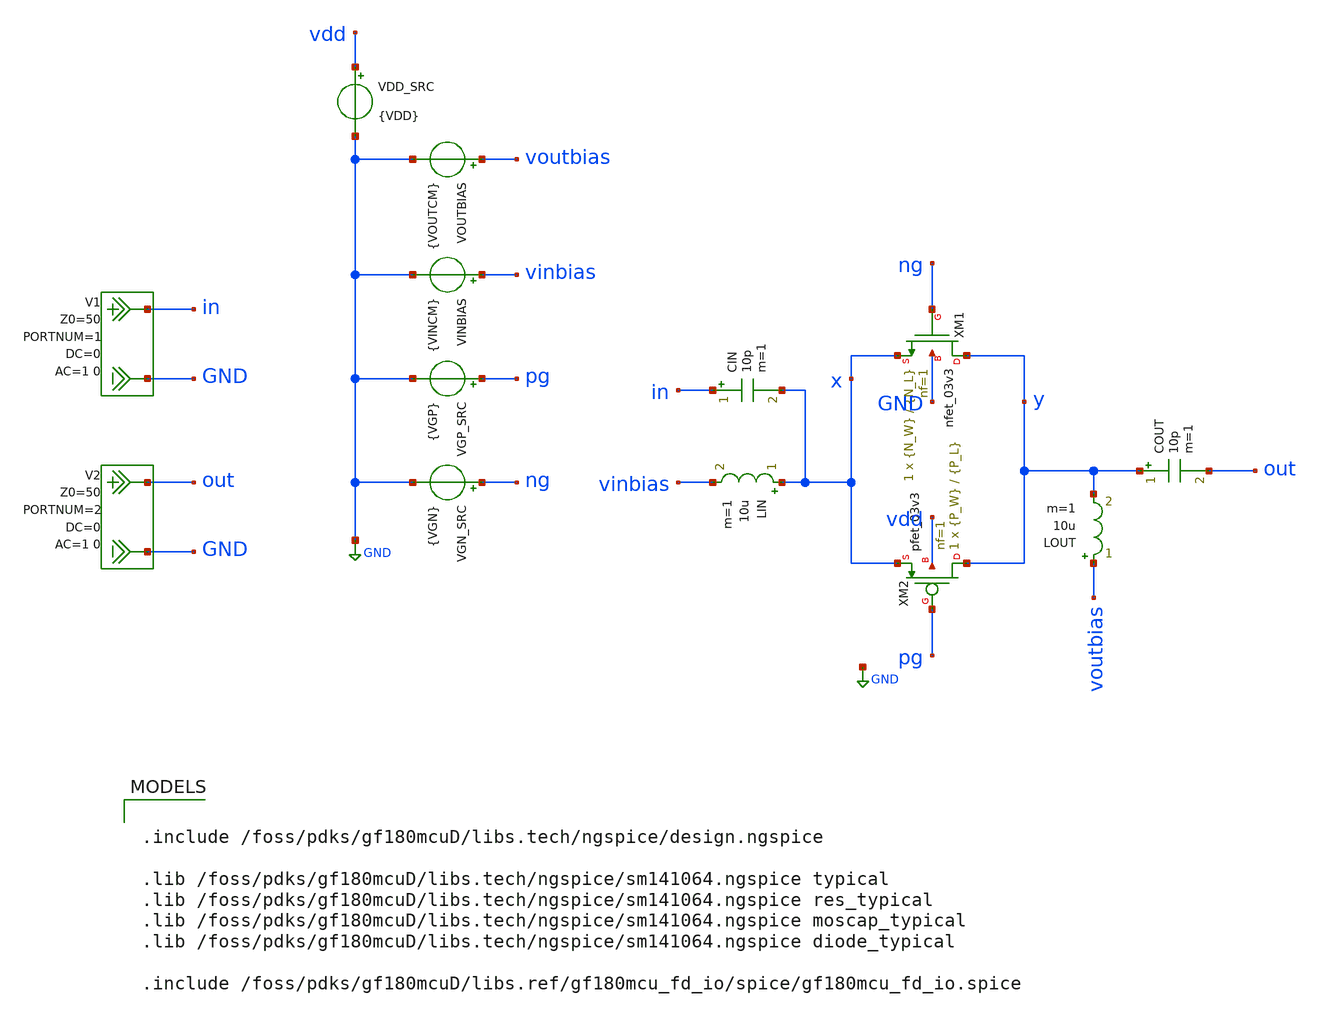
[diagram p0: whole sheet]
** sch_path: NFmin_Simulation/simulations/03_cmos/nfmin_jd_cmos_tg_cg.sch
**.subckt nfmin_jd_cmos_tg_cg
VGN_SRC ng GND {VGN}
VDD_SRC vdd GND {VDD}
COUT y out 10p m=1
CIN in x 10p m=1
XM2 y pg x vdd pfet_03v3 L={P_L} W={P_W} nf=1 ad='int((nf+1)/2) * W/nf * 0.18u' as='int((nf+2)/2) * W/nf * 0.18u'
+ pd='2*int((nf+1)/2) * (W/nf + 0.18u)' ps='2*int((nf+2)/2) * (W/nf + 0.18u)' nrd='0.18u / W' nrs='0.18u / W'
+ sa=0 sb=0 sd=0 m=1
XM1 y ng x GND nfet_03v3 L={N_L} W={N_W} nf=1 ad='int((nf+1)/2) * W/nf * 0.18u' as='int((nf+2)/2) * W/nf * 0.18u'
+ pd='2*int((nf+1)/2) * (W/nf + 0.18u)' ps='2*int((nf+2)/2) * (W/nf + 0.18u)' nrd='0.18u / W' nrs='0.18u / W'
+ sa=0 sb=0 sd=0 m=1
V1 in GND DC 0 AC 1 0 portnum 1 z0 50
V2 out GND DC 0 AC 1 0 portnum 2 z0 50
LIN x vinbias 10u m=1
VGP_SRC pg GND {VGP}
VINBIAS vinbias GND {VINCM}
VOUTBIAS voutbias GND {VOUTCM}
LOUT voutbias y 10u m=1
**** begin user architecture code

.include /foss/pdks/gf180mcuD/libs.tech/ngspice/design.ngspice

.lib /foss/pdks/gf180mcuD/libs.tech/ngspice/sm141064.ngspice typical
.lib /foss/pdks/gf180mcuD/libs.tech/ngspice/sm141064.ngspice res_typical
.lib /foss/pdks/gf180mcuD/libs.tech/ngspice/sm141064.ngspice moscap_typical
.lib /foss/pdks/gf180mcuD/libs.tech/ngspice/sm141064.ngspice diode_typical

.include /foss/pdks/gf180mcuD/libs.ref/gf180mcu_fd_io/spice/gf180mcu_fd_io.spice



.option savecurrents

.param fnoicor=0
.param sw_stat_mismatch=0

.param VDD=1.8

.param VINCM=0.9
.param VOUTCM=0.9

.param VGN=1.3
.param VGP=0.5

.param N_W=1e-6
.param N_L=0.28e-6
.param P_W=1e-6
.param P_L=0.28e-6

.control
  set noaskquit
  save all

  echo N_W_m N_L_m P_W_m P_L_m VCM VON VGN VGP VX_DC VY_DC VXY_DC IVINBIAS_A IVOUTBIAS_A IVDD_A
+ IBIAS_EQ_A JD_EQ_mA_per_um > cmos_tg_cg_jd_dense.txt
  echo N_W_m N_L_m P_W_m P_L_m VCM VON VGN VGP NFmin_dB NF_dB Rn SOpt_real SOpt_imag >
+ cmos_tg_cg_nf_dense.txt

  foreach nwval 0.22e-6 1e-6 5e-6 10e-6

    foreach pwval 0.66e-6 2e-6 10e-6 20e-6

      foreach nlval 0.28e-6 0.36e-6 0.50e-6

        foreach plval 0.28e-6 0.36e-6 0.50e-6

          let vcm = 0.90
          let von = 0.35

          while von le 0.9001

            alterparam N_W = $nwval
            alterparam P_W = $pwval
            alterparam N_L = $nlval
            alterparam P_L = $plval

            alterparam VINCM = $&vcm
            alterparam VOUTCM = $&vcm

            let vgn_set = vcm + von
            let vgp_set = vcm - von

            alterparam VGN = $&vgn_set
            alterparam VGP = $&vgp_set

            reset

            op

            let vx_dc = v(x)
            let vy_dc = v(y)
            let vxy_dc = v(y) - v(x)

            let ivin = abs(i(vinbias))
            let ivout = abs(i(voutbias))
            let ivdd = abs(i(vdd_src))

            let ibias_eq = ivin + ivout + ivdd
            let jd_eq = 1e-3*ibias_eq/($nwval + $pwval)

            echo $nwval $nlval $pwval $plval $&vcm $&von $&vgn_set $&vgp_set $&vx_dc $&vy_dc
+ $&vxy_dc $&ivin $&ivout $&ivdd $&ibias_eq $&jd_eq >> cmos_tg_cg_jd_dense.txt

            sp lin 1 2.4e9 2.4e9 1

            let nfmin_val = real(NFmin)
            let nf_val = real(NF)
            let rn_val = real(Rn)
            let sopt_re = real(SOpt)
            let sopt_im = imag(SOpt)

            echo $nwval $nlval $pwval $plval $&vcm $&von $&vgn_set $&vgp_set $&nfmin_val $&nf_val
+ $&rn_val $&sopt_re $&sopt_im >> cmos_tg_cg_nf_dense.txt

            let von = von + 0.005

          end
        end
      end
    end
  end

.endc



**** end user architecture code
**.ends
.GLOBAL GND
.end
